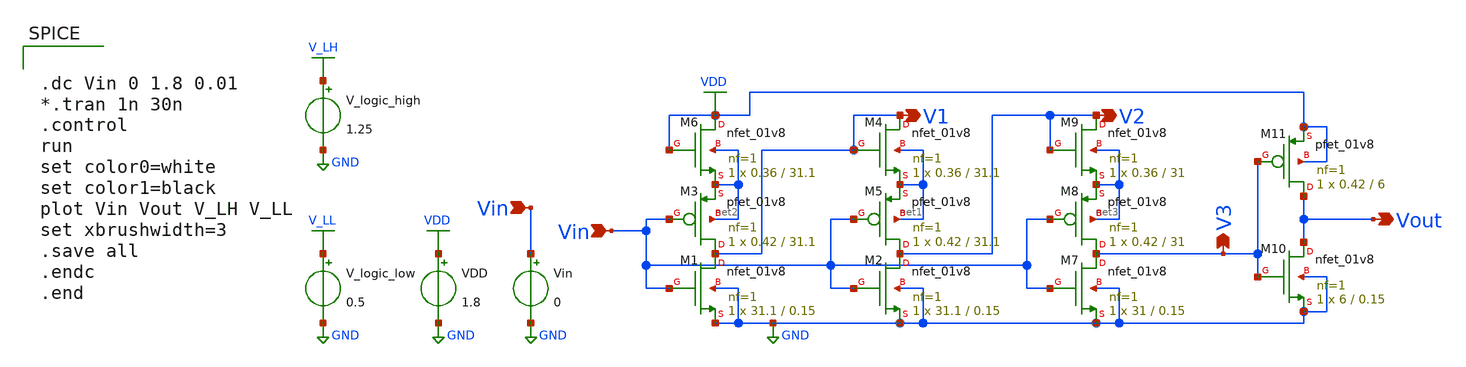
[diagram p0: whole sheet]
** sch_path: xschem/Vth_sch/th1.sch
**.subckt th1 Vin Vin V1 Vout V2 V3
*.ipin Vin
*.ipin Vin
*.opin V1
*.opin Vout
*.opin V2
*.opin V3
VDD VDD GND 1.8
Vin Vin GND 0
XM2 V2 Vin GND GND sky130_fd_pr__nfet_01v8 L=0.15 W=31.1 nf=1 ad='int((nf+1)/2) * W/nf * 0.29' as='int((nf+2)/2) * W/nf * 0.29'
+ pd='2*int((nf+1)/2) * (W/nf + 0.29)' ps='2*int((nf+2)/2) * (W/nf + 0.29)' nrd='0.29 / W' nrs='0.29 / W'
+ sa=0 sb=0 sd=0 mult=1 m=1
V_logic_high V_LH GND 1.25
V_logic_low V_LL GND 0.5
XM5 V2 Vin net1 net1 sky130_fd_pr__pfet_01v8 L=31.1 W=0.42 nf=1 ad='int((nf+1)/2) * W/nf * 0.29' as='int((nf+2)/2) * W/nf * 0.29'
+ pd='2*int((nf+1)/2) * (W/nf + 0.29)' ps='2*int((nf+2)/2) * (W/nf + 0.29)' nrd='0.29 / W' nrs='0.29 / W'
+ sa=0 sb=0 sd=0 mult=1 m=1
XM1 V1 Vin GND GND sky130_fd_pr__nfet_01v8 L=0.15 W=31.1 nf=1 ad='int((nf+1)/2) * W/nf * 0.29' as='int((nf+2)/2) * W/nf * 0.29'
+ pd='2*int((nf+1)/2) * (W/nf + 0.29)' ps='2*int((nf+2)/2) * (W/nf + 0.29)' nrd='0.29 / W' nrs='0.29 / W'
+ sa=0 sb=0 sd=0 mult=1 m=1
XM3 V1 Vin net2 net2 sky130_fd_pr__pfet_01v8 L=31.1 W=0.42 nf=1 ad='int((nf+1)/2) * W/nf * 0.29' as='int((nf+2)/2) * W/nf * 0.29'
+ pd='2*int((nf+1)/2) * (W/nf + 0.29)' ps='2*int((nf+2)/2) * (W/nf + 0.29)' nrd='0.29 / W' nrs='0.29 / W'
+ sa=0 sb=0 sd=0 mult=1 m=1
XM4 V1 V1 net1 net1 sky130_fd_pr__nfet_01v8 L=31.1 W=0.36 nf=1 ad='int((nf+1)/2) * W/nf * 0.29' as='int((nf+2)/2) * W/nf * 0.29'
+ pd='2*int((nf+1)/2) * (W/nf + 0.29)' ps='2*int((nf+2)/2) * (W/nf + 0.29)' nrd='0.29 / W' nrs='0.29 / W'
+ sa=0 sb=0 sd=0 mult=1 m=1
XM6 VDD VDD net2 net2 sky130_fd_pr__nfet_01v8 L=31.1 W=0.36 nf=1 ad='int((nf+1)/2) * W/nf * 0.29' as='int((nf+2)/2) * W/nf * 0.29'
+ pd='2*int((nf+1)/2) * (W/nf + 0.29)' ps='2*int((nf+2)/2) * (W/nf + 0.29)' nrd='0.29 / W' nrs='0.29 / W'
+ sa=0 sb=0 sd=0 mult=1 m=1
XM7 V3 Vin GND GND sky130_fd_pr__nfet_01v8 L=0.15 W=31 nf=1 ad='int((nf+1)/2) * W/nf * 0.29' as='int((nf+2)/2) * W/nf * 0.29'
+ pd='2*int((nf+1)/2) * (W/nf + 0.29)' ps='2*int((nf+2)/2) * (W/nf + 0.29)' nrd='0.29 / W' nrs='0.29 / W'
+ sa=0 sb=0 sd=0 mult=1 m=1
XM8 V3 Vin net3 net3 sky130_fd_pr__pfet_01v8 L=31 W=0.42 nf=1 ad='int((nf+1)/2) * W/nf * 0.29' as='int((nf+2)/2) * W/nf * 0.29'
+ pd='2*int((nf+1)/2) * (W/nf + 0.29)' ps='2*int((nf+2)/2) * (W/nf + 0.29)' nrd='0.29 / W' nrs='0.29 / W'
+ sa=0 sb=0 sd=0 mult=1 m=1
XM9 V2 V2 net3 net3 sky130_fd_pr__nfet_01v8 L=31 W=0.36 nf=1 ad='int((nf+1)/2) * W/nf * 0.29' as='int((nf+2)/2) * W/nf * 0.29'
+ pd='2*int((nf+1)/2) * (W/nf + 0.29)' ps='2*int((nf+2)/2) * (W/nf + 0.29)' nrd='0.29 / W' nrs='0.29 / W'
+ sa=0 sb=0 sd=0 mult=1 m=1
XM10 Vout V3 GND GND sky130_fd_pr__nfet_01v8 L=0.15 W=6 nf=1 ad='int((nf+1)/2) * W/nf * 0.29' as='int((nf+2)/2) * W/nf * 0.29'
+ pd='2*int((nf+1)/2) * (W/nf + 0.29)' ps='2*int((nf+2)/2) * (W/nf + 0.29)' nrd='0.29 / W' nrs='0.29 / W'
+ sa=0 sb=0 sd=0 mult=1 m=1
XM11 Vout V3 VDD VDD sky130_fd_pr__pfet_01v8 L=6 W=0.42 nf=1 ad='int((nf+1)/2) * W/nf * 0.29' as='int((nf+2)/2) * W/nf * 0.29'
+ pd='2*int((nf+1)/2) * (W/nf + 0.29)' ps='2*int((nf+2)/2) * (W/nf + 0.29)' nrd='0.29 / W' nrs='0.29 / W'
+ sa=0 sb=0 sd=0 mult=1 m=1
**** begin user architecture code


.lib /usr/local/share/pdk/sky130A/libs.tech/ngspice/sky130.lib.spice tt

.save all





.dc Vin 0 1.8 0.01
*.tran 1n 30n
.control
run
set color0=white
set color1=black
plot Vin Vout V_LH V_LL
set xbrushwidth=3
.save all
.endc
.end


**** end user architecture code
**.ends
.GLOBAL VDD
.GLOBAL GND
.GLOBAL V_LH
.GLOBAL V_LL
.end
